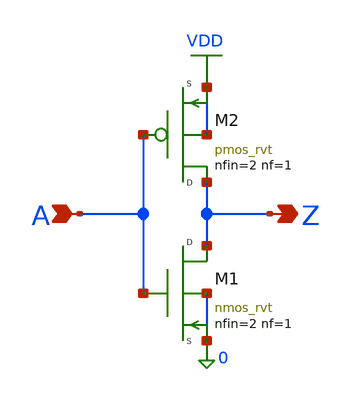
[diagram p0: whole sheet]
** sch_path: tests/klayout/inv_globals.sch
**.subckt inv_globals A Z
*.ipin A
*.opin Z
NM1 Z A 0 0 nmos_rvt l=20n nfin=2 nf=1 m=1
NM2 Z A VDD VDD pmos_rvt l=20n nfin=2 nf=1 m=1
**.ends
.GLOBAL VDD
.end
